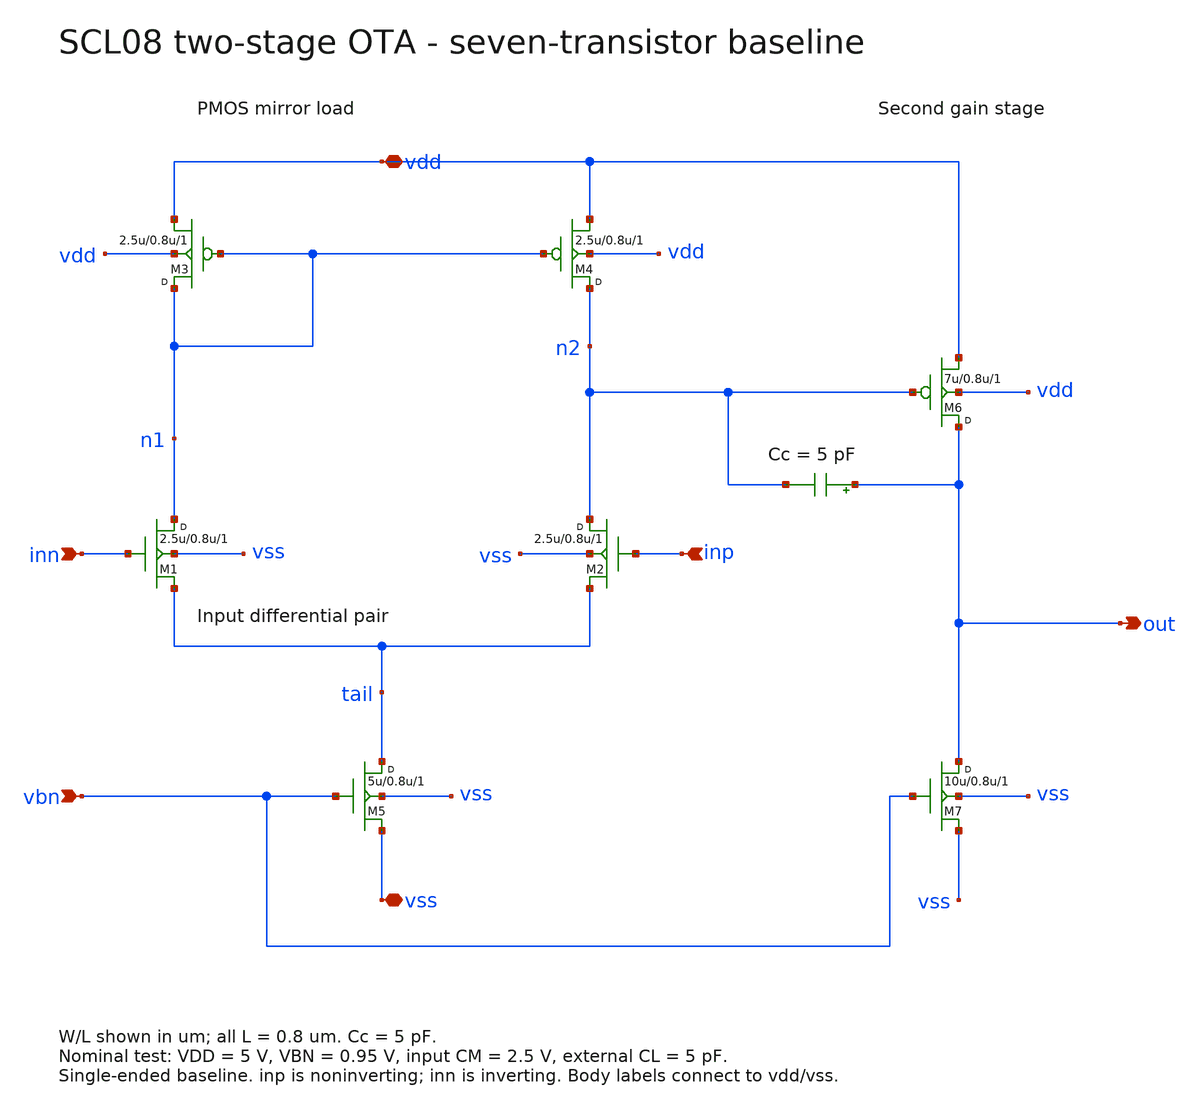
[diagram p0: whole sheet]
** sch_path: OTA/design_1/designs/ota_scl08.sch
**.subckt ota_scl08 inp inn out vdd vss vbn
*.ipin inp
*.ipin inn
*.opin out
*.iopin vdd
*.iopin vss
*.ipin vbn
M3 n1 n1 vdd vdd P w=2.5u l=0.8u m=1
M4 n2 n1 vdd vdd P w=2.5u l=0.8u m=1
M1 n1 inn tail vss N w=2.5u l=0.8u m=1
M2 n2 inp tail vss N w=2.5u l=0.8u m=1
M5 tail vbn vss vss N w=5u l=0.8u m=1
M6 out n2 vdd vdd P w=7u l=0.8u m=1
M7 out vbn vss vss N w=10u l=0.8u m=1
Cc out n2 5p m=1
**.ends
.end
